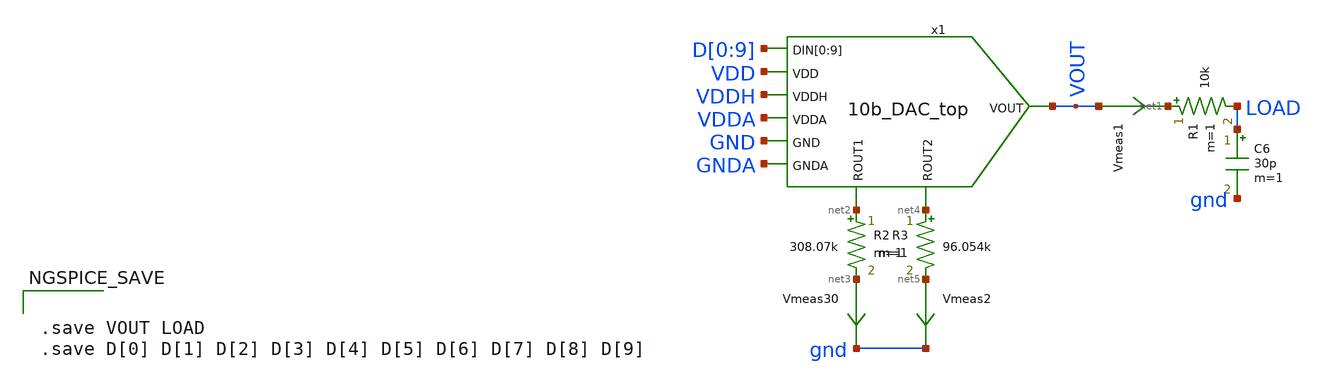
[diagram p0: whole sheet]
** sch_path: xschem/10b_DAC-tb.sch
.lib $::SKYWATER_MODELS/sky130.lib.spice tt
.include $::SKYWATER_STDCELLS/sky130_fd_sc_hd.spice

**.subckt 10b_DAC-tb
C6 LOAD gnd 30p m=1
R1 net1 LOAD 10k m=1
Vmeas1 VOUT net1 0
.save i(vmeas1)
R2 net2 net3 308.07k m=1
Vmeas30 net3 gnd 0
.save i(vmeas30)
R3 net4 net5 96.054k m=1
Vmeas2 net5 gnd 0
.save i(vmeas2)
x1 D[0] D[1] D[2] D[3] D[4] D[5] D[6] D[7] D[8] D[9] VDD VDDH VDDA GND GNDA VOUT net2 net4
+ 10b_DAC_top
**** begin user architecture code



  .option wnflag=1
  .option safecurrents
  ********************Static Voltage Sources***************************
  Vddh vddh gnd dc 5.5
  Vdd vdd gnd dc 1.8
  Vdda vdda gnd dc 5.5
  Vgnda gnda gnd dc 0
  ********************Dynamic Voltage Sources***************************
  *******Calculation**********
  .param base_f=100e3 base_t={1/base_f} base_th={base_t/2} base_d={base_th}
  .param d0_th={base_th} d0_t={d0_th*2}
  .param d1_th={d0_th*2} d1_t={d1_th*2}
  .param d2_th={d1_th*2} d2_t={d2_th*2}
  .param d3_th={d2_th*2} d3_t={d3_th*2}
  .param d4_th={d3_th*2} d4_t={d4_th*2}
  .param d5_th={d4_th*2} d5_t={d5_th*2}
  .param d6_th={d5_th*2} d6_t={d6_th*2}
  .param d7_th={d6_th*2} d7_t={d7_th*2}
  .param d8_th={d7_th*2} d8_t={d8_th*2}
  .param d9_th={d8_th*2} d9_t={d9_th*2}
  *******Signals**********
  .param vhi=1.8
  Vd0  d[0]  gnd pulse({vhi} 0 {base_d} 1n 1n {d0_th} {d0_t})
  Vd1  d[1]  gnd pulse({vhi} 0 {base_d} 1n 1n {d1_th} {d1_t})
  Vd2  d[2]  gnd pulse({vhi} 0 {base_d} 1n 1n {d2_th} {d2_t})
  Vd3  d[3]  gnd pulse({vhi} 0 {base_d} 1n 1n {d3_th} {d3_t})
  Vd4  d[4]  gnd pulse({vhi} 0 {base_d} 1n 1n {d4_th} {d4_t})
  Vd5  d[5]  gnd pulse({vhi} 0 {base_d} 1n 1n {d5_th} {d5_t})
  *Vd6  d[6]  gnd pulse({vhi} 0 {base_d} 1n 1n {d6_th} {d6_t})
  *Vd7  d[7]  gnd pulse({vhi} 0 {base_d} 1n 1n {d7_th} {d7_t})
  *Vd8  d[8]  gnd pulse({vhi} 0 {base_d} 1n 1n {d8_th} {d8_t})
  *Vd9  d[9]  gnd pulse({vhi} 0 {base_d} 1n 1n {d9_th} {d9_t})

  Vd6  d[6]  gnd vhi
  Vd7  d[7]  gnd vhi
  Vd8  d[8]  gnd 0
  Vd9  d[9]  gnd vhi
  ********************Simulation Commands*****************************
  .control
     reset
     tran 1n 100u
     write 10b_DAC-tb.raw
     set appendwrite
*    quit 0
  .endc





.save VOUT LOAD
.save D[0] D[1] D[2] D[3] D[4] D[5] D[6] D[7] D[8] D[9]


**** end user architecture code
**.ends
.end
